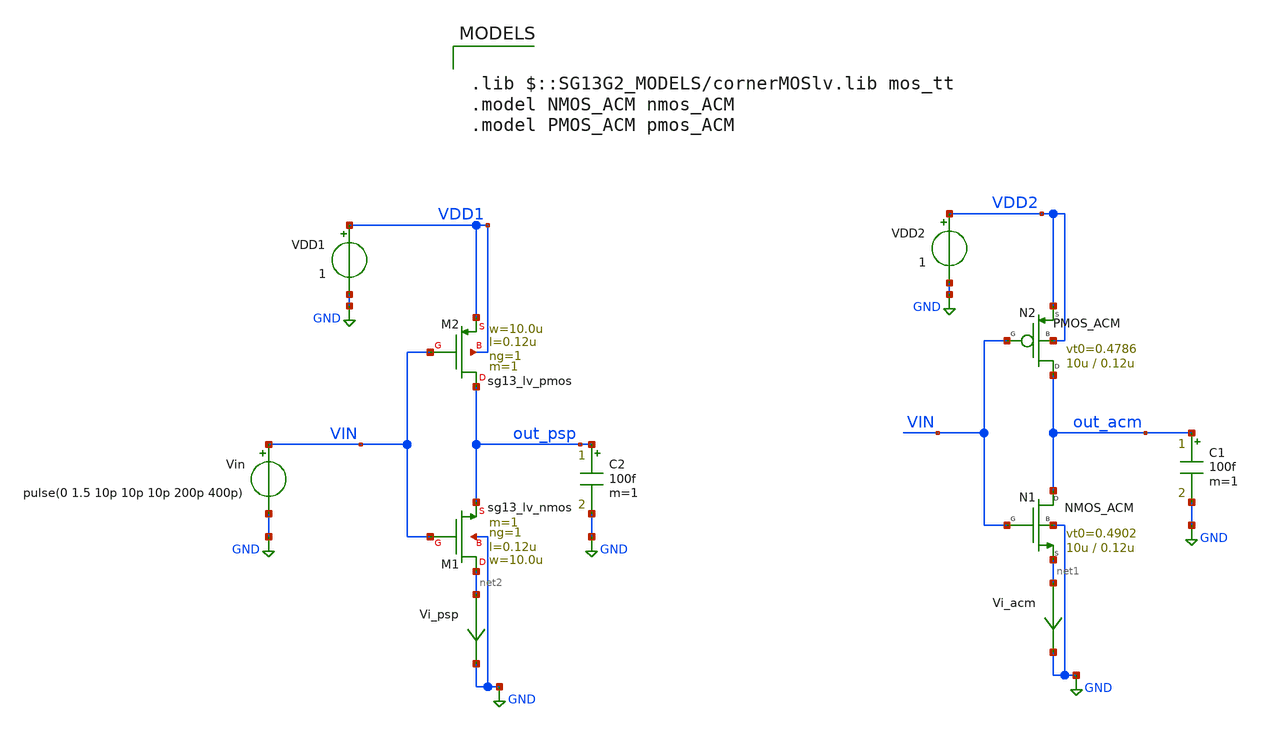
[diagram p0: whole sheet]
** sch_path: ihp_tutorials/inverter_acm.sch
**.subckt inverter_acm
VDD1 VDD1 GND 1
XM1 net2 VIN out_psp GND sg13_lv_nmos w=10.0u l=0.12u ng=1 m=1 mm_ok=1
XM2 out_psp VIN VDD1 VDD1 sg13_lv_pmos w=10.0u l=0.12u ng=1 m=1 mm_ok=1
VDD2 VDD2 GND 1
N1 out_acm VIN net1 GND NMOS_ACM w=10u l=0.12u n=1.414 is=11.77u vt0=0.4902 sigma=53.4m zeta=7m
N2 out_acm VIN VDD2 VDD2 PMOS_ACM w=10u l=0.12u n=1.466 is=9.391u vt0=0.4786 sigma=48.4m zeta=31m
Vin VIN GND pulse(0 1.5 10p 10p 10p 200p 400p)
Vi_psp net2 GND 0
.save i(vi_psp)
Vi_acm net1 GND 0
.save i(vi_acm)
C1 out_acm GND 100f m=1
C2 out_psp GND 100f m=1
**** begin user architecture code



.control
pre_osdi ./psp103_nqs.osdi
pre_osdi ./NMOS_ACM_2V0.osdi
pre_osdi ./PMOS_ACM_2V0.osdi
save all

remzerovec
tran 1p 100p
write inverter_acm.raw
*wrdata /home/gmaranhao/Desktop/ihp130_work/Inverter_data/inverter_tran_1p5_W10u0_L0u12_V_PSP.txt
*+ V(out_psp)
*wrdata /home/gmaranhao/Desktop/ihp130_work/Inverter_data/inverter_tran_1p5_W10u0_L0u12_I_PSP.txt
*+ i(Vi_psp)
*wrdata /home/gmaranhao/Desktop/ihp130_work/Inverter_data/inverter_tran_1p5_W10u0_L0u12_V_ACM.txt
*+ V(out_acm)
*wrdata /home/gmaranhao/Desktop/ihp130_work/Inverter_data/inverter_tran_1p5_W10u0_L0u12_I_ACM.txt
*+ i(Vi_acm)
*wrdata
*+ /home/gmaranhao/Desktop/ihp130_work/Inverter_data/inverter_tran_1p5_W10u0_L0u12_I_ACM_vin.txt V(VIN)

set appendwrite

remzerovec
dc Vin 0 1 10m
write inverter_acm.raw
*wrdata /home/gmaranhao/Desktop/ihp130_work/Inverter_data/inverter_DC_1p0_W10u0_L0u12_V_PSP.txt
*+ V(out_psp)
*wrdata /home/gmaranhao/Desktop/ihp130_work/Inverter_data/inverter_DC_1p0_W10u0_L0u12_I_PSP.txt
*+ i(Vi_psp)
*wrdata /home/gmaranhao/Desktop/ihp130_work/Inverter_data/inverter_DC_1p0_W10u0_L0u12_V_ACM.txt
*+ V(out_acm)
*wrdata /home/gmaranhao/Desktop/ihp130_work/Inverter_data/inverter_DC_1p0_W10u0_L0u12_I_ACM.txt
*+ i(Vi_acm)

.endc




.lib $::SG13G2_MODELS/cornerMOSlv.lib mos_tt
.model NMOS_ACM nmos_ACM
.model PMOS_ACM pmos_ACM

**** end user architecture code
**.ends
.GLOBAL GND
.end
